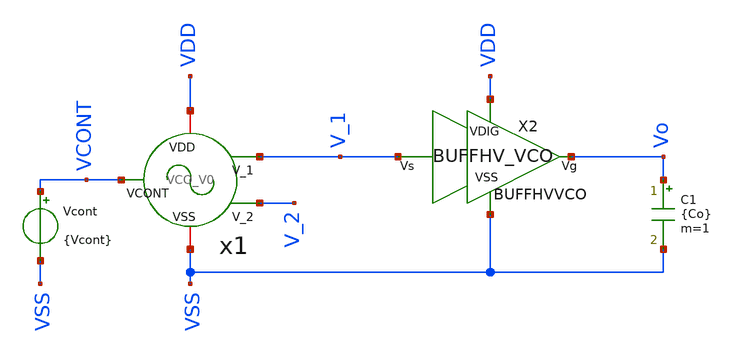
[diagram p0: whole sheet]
** sch_path: xschem/VCO/TB_VCO_V0.sch
**.subckt TB_VCO_V0
C1 Vo VSS {Co} m=1
Vcont VCONT VSS {Vcont}
X2 V_1 Vo VDD VSS BUFFHVVCO
x1 VCONT VSS VDD V_1 V_2 VCO_V0
**** begin user architecture code

.param Co = 4*0.28f
.param mult = 1
.param w_inv = 0.15u
.param l_inv = 0.15u

*.param Vcont = 0.8
.param VCP = 0.57
.param VCN = 0.76

vvdd vdd 0 dc 3.3
vvss vss 0 0
*vvcont VCONT 0 dc 0
*vvcont2 VCONT2 0 dc 0
*.option temp = 200
.ic v(V_1) = 0
.ic v(V_2) = 3.3
*.ic v(V_11) = 0
*.ic v(V_22) = 3.3
.save v(V_1) v(Vo)

.param fmin = 7.5Meg
*.param fmin = 1Meg
.param Tmin = 1/fmin
.param SimTime =  Tmin*20
.csparam SimTime ={Simtime}
.csparam Tmargin = Tmin*2





.save all
.tran 10n {SimTime}
.csparam start = 10
.param Vcont = 0
.control
let Vtarg = 1.5
compose vin_var start=0 stop=2 step=0.2

.param fsw = 5Meg
.param Vmax = 2
.param VDD = 3.3
.param Vscaling = Vmax/VDD
.param Vref = 1.2
.param KiObj = 0.5Meg
.param fcObj = fsw -KiObj*(Vref*Vscaling-Vmax/2)
.csparam fcObj = {fcObj}


let strt = 0
let stp = 2
let step = 0.2
let len2 = 1 + (stp-strt)/step
let f_sweep = vector(len2)
let index = 0
foreach val $&vin_var
	alter vcont $val
	let f_sum = 0
	let t_act = 0
	let period_cont = 3
	let period_cont2 = 4
	run

	meas tran T0 TRIG v(Vo) VAL = {Vtarg} RISE = 1 TARG v(Vo) VAL = {Vtarg}  RISE = 2
	let Tmargin = T0*2
	while t_act le SimTime - Tmargin
		meas tran t_rise WHEN v(Vo) = {Vtarg} RISE = {period_cont}
		let t_act = t_rise
		*print t_act SimTime period_cont
		meas tran T TRIG v(Vo) VAL = {Vtarg} RISE = {period_cont} TARG v(Vo) VAL = {Vtarg}  RISE = {period_cont2}
		let f =1/T
		let f_sum = f_sum + f
		let period_cont = period_cont + 1
		let period_cont2 = period_cont2 + 1
	end
	*wrdata ../../sim_data/data_VCO_vto1p1.txt tran1.v(V_1) tran2.v(V_1) tran3.v(V_1) tran4.v(V_1)
+ tran5.v(V_1) tran6.v(V_1) tran7.v(V_1) tran8.v(V_1) tran9.v(V_1) tran10.v(V_1) tran11.v(V_1) tran12.v(V_1)
+ tran13.v(V_1) tran14.v(V_1) tran15.v(V_1) tran16.v(V_1) tran17.v(V_1)
	let f_avg = f_sum/(period_cont-3)
	let f_sweep[index] = f_avg
	let index = index +1
end
plot tran1.v(Vo)
plot tran10.v(Vo)
print f_sweep
print fcObj
plot f_sweep vs vin_var
*wrdata
*+ /workspaces/usm-vlsi-tools/shared_xserver/simulations/SKY130/IPD500-TimebasedDCDCBuck/sim_data/data_VCO_sky130.txt tran1.v(V_1) tran2.v(V_1) tran3.v(V_1) tran4.v(V_1) tran5.v(V_1) tran6.v(V_1) tran7.v(V_1)
*+ tran8.v(V_1) tran9.v(V_1) tran10.v(V_1) tran11.v(V_1)
*wrdata
*+ /workspaces/usm-vlsi-tools/shared_xserver/simulations/SKY130/IPD500-TimebasedDCDCBuck/sim_data/data_fsweep.txt f_sweep[1] vin_var
.endc




.lib cornerMOShv.lib mos_tt
.lib cornerMOSlv.lib mos_tt
*.lib cornerMOShv.lib mos_ff
*.lib cornerMOSlv.lib mos_ff
*.lib cornerMOShv.lib mos_ss
*.lib cornerMOSlv.lib mos_ss
*.lib cornerMOShv.lib mos_sf
*.lib cornerMOSlv.lib mos_sf
*.lib cornerMOShv.lib mos_fs
*.lib cornerMOSlv.lib mos_fs

*.include /opt/pdks/ihp-sg13g2/libs.ref/sg13g2_stdcell/spice/sg13g2_stdcell.spice
*.lib $::SG13G2_MODELS/cornerRES.lib res_typ
*.lib $::SG13G2_MODELS/cornerCAP.lib cap_typ
*.lib $::SG13G2_MODELS/diodes.lib




.option KLU
*.option itl4=100
.option method=gear
*.option maxord=2
*.option trtol=25
*.option lvltim=1
*.option tnum=1e9
*.option reltol=1e-3
*.option abstol=1e-10
*.option vntol=1e-4
*.option event
*.option gmin=1e-10
*.option cshunt=1e-13
.option cshunt=0.14f




.param w_MP1a = 1u
.param l_MP1a = 40u
.param w_MP1b = 1u
.param l_MP1b = 8u
.param w_MP2 = 8u
.param l_MP2 = 4u
.param w_MP3 = 7u
.param l_MP3 = 4u
.param w_MP4 = 3u
.param l_MP4 = 5u

.param w_MN1 = 6u
.param l_MN1 = 0.5u
.param w_MN2 = 5u
.param l_MN2 = 0.5u
.param w_MN3 = 4u
.param l_MN3 = 0.5u
.param w_MN4 = 2u
.param l_MN4 = 5u




**** end user architecture code
**.ends
.end
